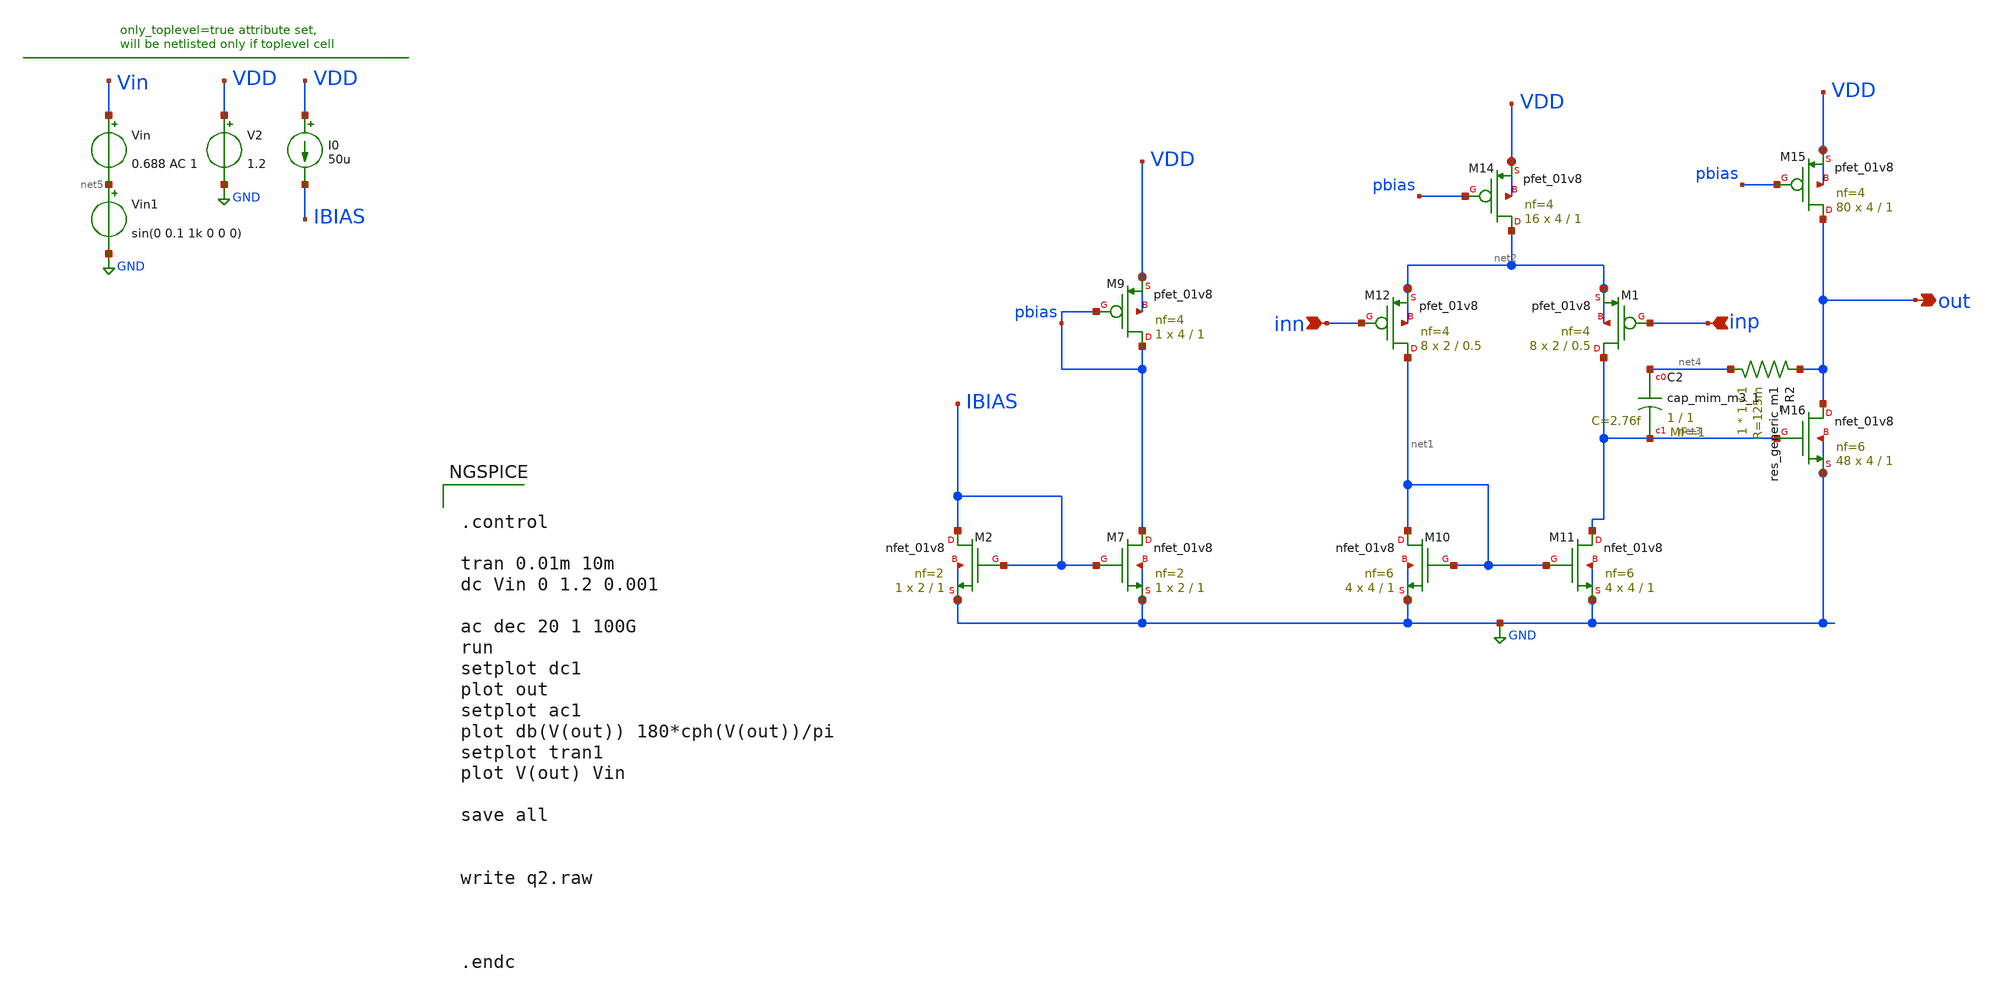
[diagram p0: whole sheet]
** sch_path: archive/q2_opamp.sch
**.subckt q2_opamp inn inp out
*.ipin inn
*.ipin inp
*.opin out
Vin Vin net5 0.688 AC 1
V2 VDD GND 1.2
Vin1 net5 GND sin(0 0.1 1k 0 0 0)
XM2 IBIAS IBIAS GND GND sky130_fd_pr__nfet_01v8 L=1 W=2 nf=2 ad='int((nf+1)/2) * W/nf * 0.29' as='int((nf+2)/2) * W/nf * 0.29'
+ pd='2*int((nf+1)/2) * (W/nf + 0.29)' ps='2*int((nf+2)/2) * (W/nf + 0.29)' nrd='0.29 / W' nrs='0.29 / W'
+ sa=0 sb=0 sd=0 mult=1 m=1
XM7 pbias IBIAS GND GND sky130_fd_pr__nfet_01v8 L=1 W=2 nf=2 ad='int((nf+1)/2) * W/nf * 0.29' as='int((nf+2)/2) * W/nf * 0.29'
+ pd='2*int((nf+1)/2) * (W/nf + 0.29)' ps='2*int((nf+2)/2) * (W/nf + 0.29)' nrd='0.29 / W' nrs='0.29 / W'
+ sa=0 sb=0 sd=0 mult=1 m=1
I0 VDD IBIAS 50u
XM9 pbias pbias VDD VDD sky130_fd_pr__pfet_01v8 L=1 W=4 nf=4 ad='int((nf+1)/2) * W/nf * 0.29' as='int((nf+2)/2) * W/nf * 0.29'
+ pd='2*int((nf+1)/2) * (W/nf + 0.29)' ps='2*int((nf+2)/2) * (W/nf + 0.29)' nrd='0.29 / W' nrs='0.29 / W'
+ sa=0 sb=0 sd=0 mult=1 m=1
XM10 net1 net1 GND GND sky130_fd_pr__nfet_01v8 L=1 W=4 nf=6 ad='int((nf+1)/2) * W/nf * 0.29' as='int((nf+2)/2) * W/nf * 0.29'
+ pd='2*int((nf+1)/2) * (W/nf + 0.29)' ps='2*int((nf+2)/2) * (W/nf + 0.29)' nrd='0.29 / W' nrs='0.29 / W'
+ sa=0 sb=0 sd=0 mult=4 m=4
XM11 net3 net1 GND GND sky130_fd_pr__nfet_01v8 L=1 W=4 nf=6 ad='int((nf+1)/2) * W/nf * 0.29' as='int((nf+2)/2) * W/nf * 0.29'
+ pd='2*int((nf+1)/2) * (W/nf + 0.29)' ps='2*int((nf+2)/2) * (W/nf + 0.29)' nrd='0.29 / W' nrs='0.29 / W'
+ sa=0 sb=0 sd=0 mult=4 m=4
XM12 net1 inn net2 net2 sky130_fd_pr__pfet_01v8 L=0.5 W=2 nf=4 ad='int((nf+1)/2) * W/nf * 0.29' as='int((nf+2)/2) * W/nf * 0.29'
+ pd='2*int((nf+1)/2) * (W/nf + 0.29)' ps='2*int((nf+2)/2) * (W/nf + 0.29)' nrd='0.29 / W' nrs='0.29 / W'
+ sa=0 sb=0 sd=0 mult=8 m=8
XM1 net3 inp net2 net2 sky130_fd_pr__pfet_01v8 L=0.5 W=2 nf=4 ad='int((nf+1)/2) * W/nf * 0.29' as='int((nf+2)/2) * W/nf * 0.29'
+ pd='2*int((nf+1)/2) * (W/nf + 0.29)' ps='2*int((nf+2)/2) * (W/nf + 0.29)' nrd='0.29 / W' nrs='0.29 / W'
+ sa=0 sb=0 sd=0 mult=8 m=8
XM14 net2 pbias VDD VDD sky130_fd_pr__pfet_01v8 L=1 W=4 nf=4 ad='int((nf+1)/2) * W/nf * 0.29' as='int((nf+2)/2) * W/nf * 0.29'
+ pd='2*int((nf+1)/2) * (W/nf + 0.29)' ps='2*int((nf+2)/2) * (W/nf + 0.29)' nrd='0.29 / W' nrs='0.29 / W'
+ sa=0 sb=0 sd=0 mult=16 m=16
XM15 out pbias VDD VDD sky130_fd_pr__pfet_01v8 L=1 W=4 nf=4 ad='int((nf+1)/2) * W/nf * 0.29' as='int((nf+2)/2) * W/nf * 0.29'
+ pd='2*int((nf+1)/2) * (W/nf + 0.29)' ps='2*int((nf+2)/2) * (W/nf + 0.29)' nrd='0.29 / W' nrs='0.29 / W'
+ sa=0 sb=0 sd=0 mult=80 m=80
XM16 out net3 GND GND sky130_fd_pr__nfet_01v8 L=1 W=4 nf=6 ad='int((nf+1)/2) * W/nf * 0.29' as='int((nf+2)/2) * W/nf * 0.29'
+ pd='2*int((nf+1)/2) * (W/nf + 0.29)' ps='2*int((nf+2)/2) * (W/nf + 0.29)' nrd='0.29 / W' nrs='0.29 / W'
+ sa=0 sb=0 sd=0 mult=48 m=48
R2 net4 out sky130_fd_pr__res_generic_m1 W=1 L=1 m=1
XC2 net4 net3 sky130_fd_pr__cap_mim_m3_1 W=1 L=1 MF=1 m=1
**** begin user architecture code

** opencircuitdesign pdks install
.lib $::SKYWATER_MODELS/sky130.lib.spice tt




.control

tran 0.01m 10m
dc Vin 0 1.2 0.001

ac dec 20 1 100G
run
setplot dc1
plot out
setplot ac1
plot db(V(out)) 180*cph(V(out))/pi
setplot tran1
plot V(out) Vin

save all


write q2.raw



.endc


**** end user architecture code
**.ends
.GLOBAL GND
.end
